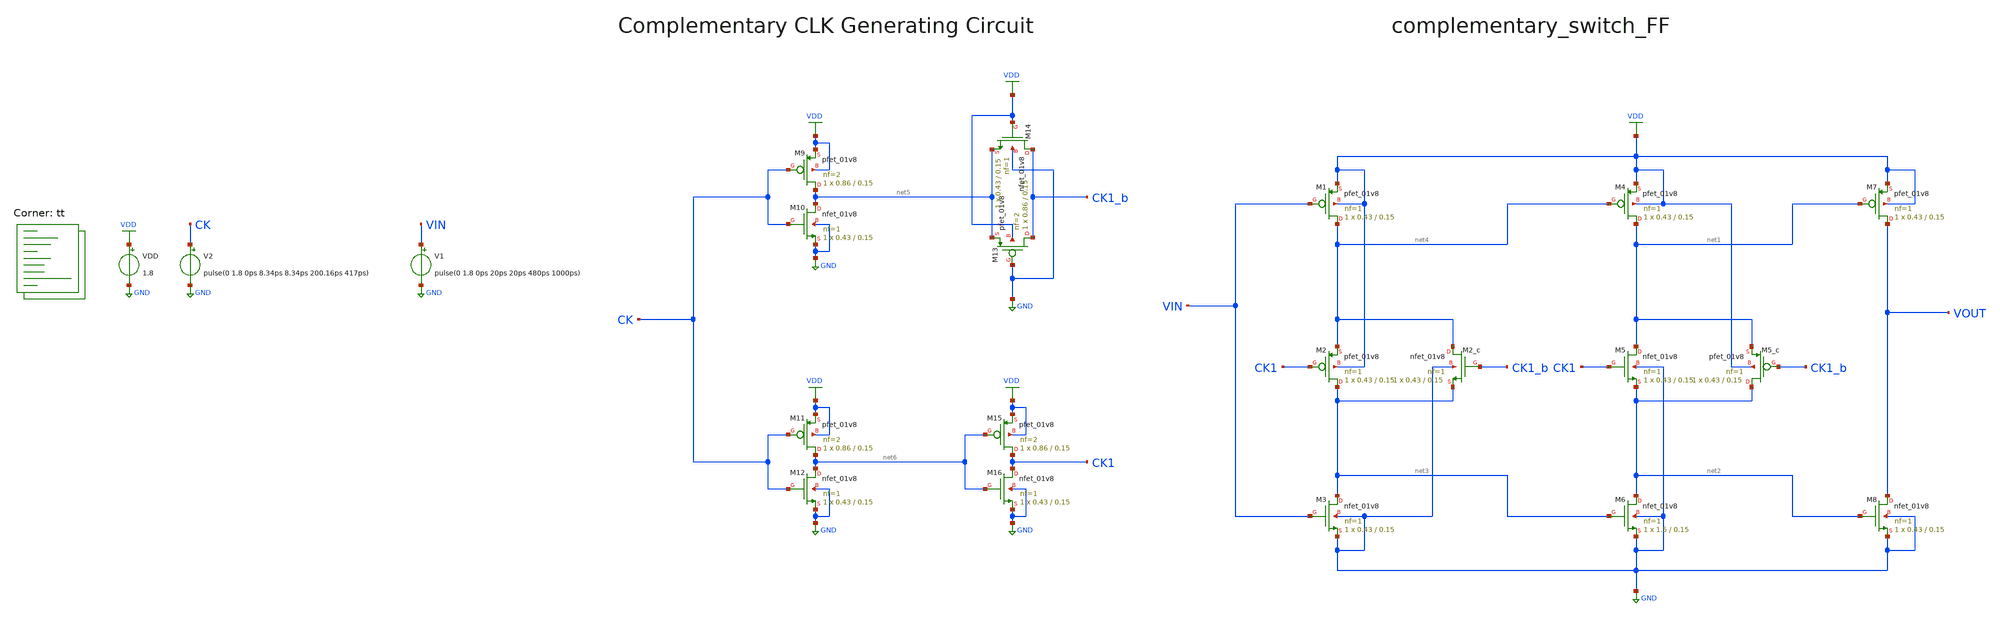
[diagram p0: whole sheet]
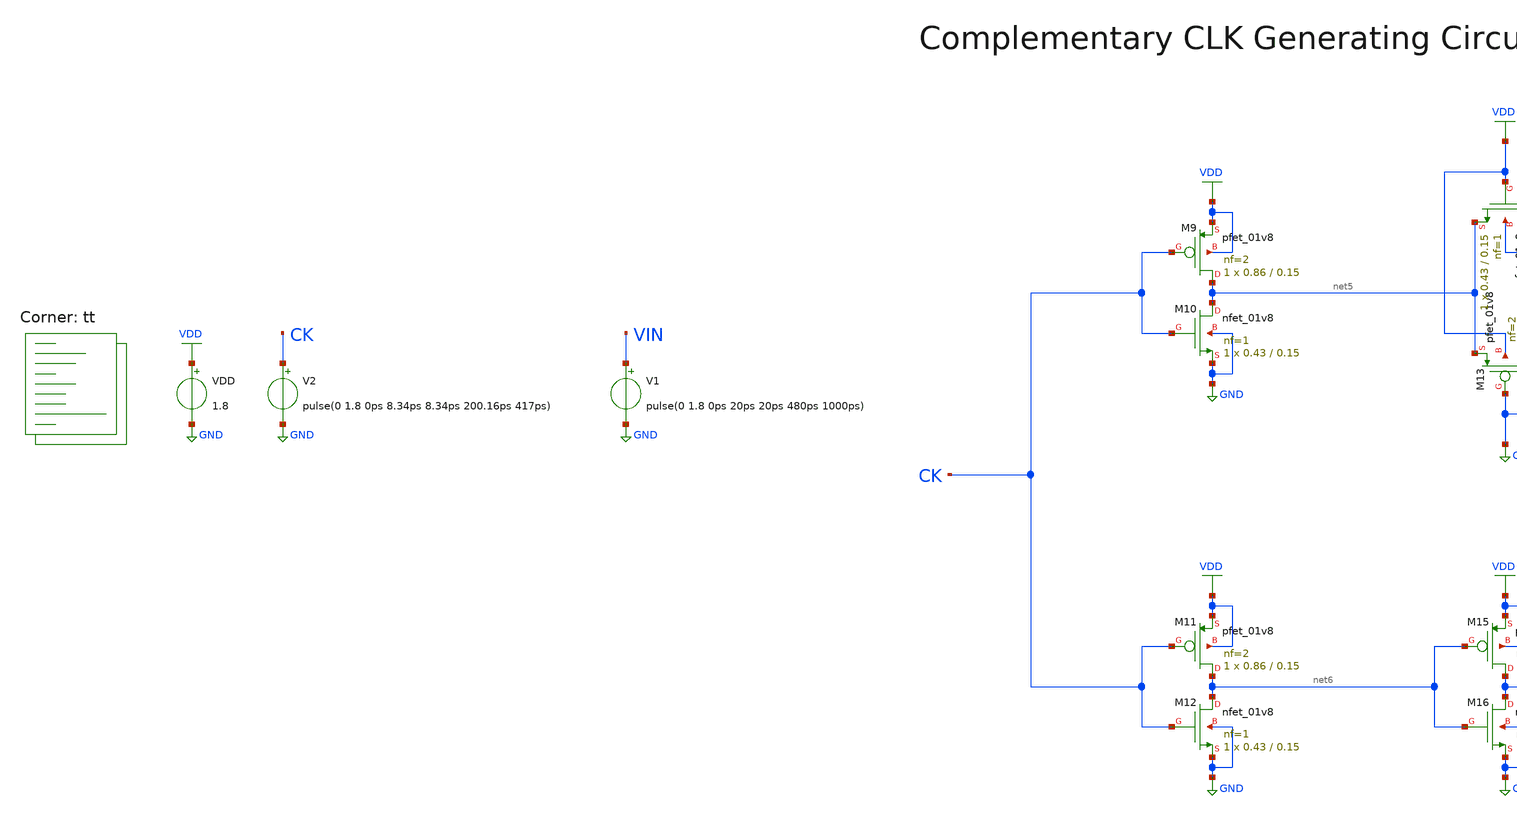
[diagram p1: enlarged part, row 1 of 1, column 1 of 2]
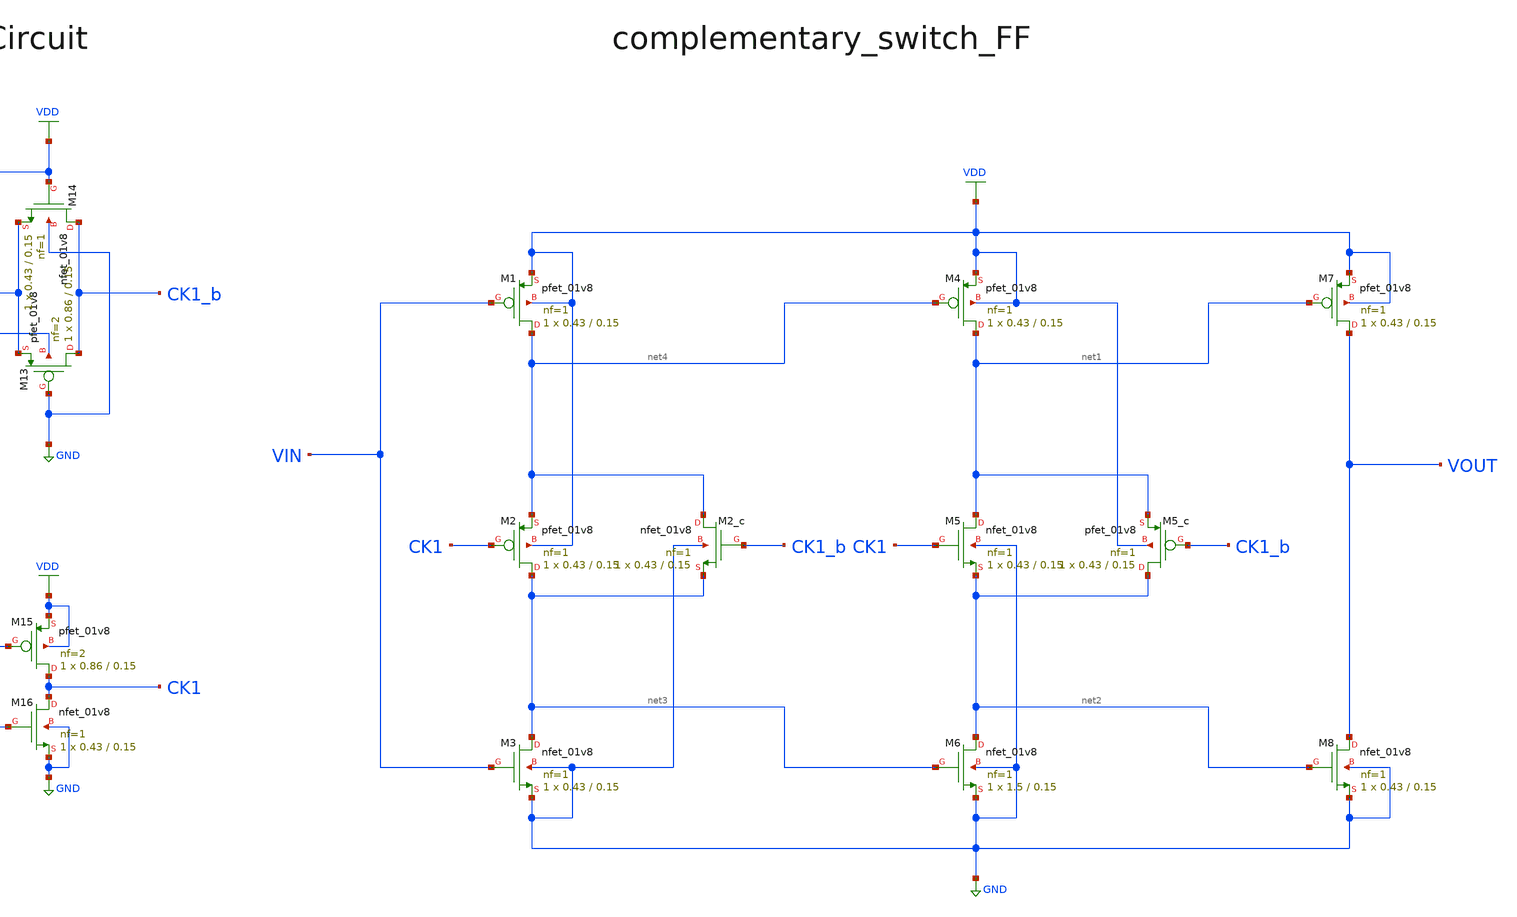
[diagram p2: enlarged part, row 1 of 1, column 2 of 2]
** sch_path: projects/pll/divider/xschem_ngspice/tb_FF_comp_sw.sch
**.subckt tb_FF_comp_sw
VDD VDD GND 1.8
V2 CK GND pulse(0 1.8 0ps 8.34ps 8.34ps 200.16ps 417ps)
XM7 VOUT net1 VDD VDD sky130_fd_pr__pfet_01v8 L=0.15 W=0.43 nf=1 ad='int((nf+1)/2) * W/nf * 0.29' as='int((nf+2)/2) * W/nf * 0.29'
+ pd='2*int((nf+1)/2) * (W/nf + 0.29)' ps='2*int((nf+2)/2) * (W/nf + 0.29)' nrd='0.29 / W' nrs='0.29 / W'
+ sa=0 sb=0 sd=0 mult=1 m=1
XM5 net1 CK1 net2 GND sky130_fd_pr__nfet_01v8 L=0.15 W=0.43 nf=1 ad='int((nf+1)/2) * W/nf * 0.29' as='int((nf+2)/2) * W/nf * 0.29'
+ pd='2*int((nf+1)/2) * (W/nf + 0.29)' ps='2*int((nf+2)/2) * (W/nf + 0.29)' nrd='0.29 / W' nrs='0.29 / W'
+ sa=0 sb=0 sd=0 mult=1 m=1
XM8 VOUT net2 GND GND sky130_fd_pr__nfet_01v8 L=0.15 W=0.43 nf=1 ad='int((nf+1)/2) * W/nf * 0.29' as='int((nf+2)/2) * W/nf * 0.29'
+ pd='2*int((nf+1)/2) * (W/nf + 0.29)' ps='2*int((nf+2)/2) * (W/nf + 0.29)' nrd='0.29 / W' nrs='0.29 / W'
+ sa=0 sb=0 sd=0 mult=1 m=1
XM4 net1 net4 VDD VDD sky130_fd_pr__pfet_01v8 L=0.15 W=0.43 nf=1 ad='int((nf+1)/2) * W/nf * 0.29' as='int((nf+2)/2) * W/nf * 0.29'
+ pd='2*int((nf+1)/2) * (W/nf + 0.29)' ps='2*int((nf+2)/2) * (W/nf + 0.29)' nrd='0.29 / W' nrs='0.29 / W'
+ sa=0 sb=0 sd=0 mult=1 m=1
XM6 net2 net3 GND GND sky130_fd_pr__nfet_01v8 L=0.15 W=1.5 nf=1 ad='int((nf+1)/2) * W/nf * 0.29' as='int((nf+2)/2) * W/nf * 0.29'
+ pd='2*int((nf+1)/2) * (W/nf + 0.29)' ps='2*int((nf+2)/2) * (W/nf + 0.29)' nrd='0.29 / W' nrs='0.29 / W'
+ sa=0 sb=0 sd=0 mult=1 m=1
XM1 net4 VIN VDD VDD sky130_fd_pr__pfet_01v8 L=0.15 W=0.43 nf=1 ad='int((nf+1)/2) * W/nf * 0.29' as='int((nf+2)/2) * W/nf * 0.29'
+ pd='2*int((nf+1)/2) * (W/nf + 0.29)' ps='2*int((nf+2)/2) * (W/nf + 0.29)' nrd='0.29 / W' nrs='0.29 / W'
+ sa=0 sb=0 sd=0 mult=1 m=1
XM3 net3 VIN GND GND sky130_fd_pr__nfet_01v8 L=0.15 W=0.43 nf=1 ad='int((nf+1)/2) * W/nf * 0.29' as='int((nf+2)/2) * W/nf * 0.29'
+ pd='2*int((nf+1)/2) * (W/nf + 0.29)' ps='2*int((nf+2)/2) * (W/nf + 0.29)' nrd='0.29 / W' nrs='0.29 / W'
+ sa=0 sb=0 sd=0 mult=1 m=1
XM2 net3 CK1 net4 VDD sky130_fd_pr__pfet_01v8 L=0.15 W=0.43 nf=1 ad='int((nf+1)/2) * W/nf * 0.29' as='int((nf+2)/2) * W/nf * 0.29'
+ pd='2*int((nf+1)/2) * (W/nf + 0.29)' ps='2*int((nf+2)/2) * (W/nf + 0.29)' nrd='0.29 / W' nrs='0.29 / W'
+ sa=0 sb=0 sd=0 mult=1 m=1
XM5_c net2 CK1_b net1 VDD sky130_fd_pr__pfet_01v8 L=0.15 W=0.43 nf=1 ad='int((nf+1)/2) * W/nf * 0.29'
+ as='int((nf+2)/2) * W/nf * 0.29' pd='2*int((nf+1)/2) * (W/nf + 0.29)' ps='2*int((nf+2)/2) * (W/nf + 0.29)'
+ nrd='0.29 / W' nrs='0.29 / W' sa=0 sb=0 sd=0 mult=1 m=1
XM2_c net4 CK1_b net3 GND sky130_fd_pr__nfet_01v8 L=0.15 W=0.43 nf=1 ad='int((nf+1)/2) * W/nf * 0.29'
+ as='int((nf+2)/2) * W/nf * 0.29' pd='2*int((nf+1)/2) * (W/nf + 0.29)' ps='2*int((nf+2)/2) * (W/nf + 0.29)'
+ nrd='0.29 / W' nrs='0.29 / W' sa=0 sb=0 sd=0 mult=1 m=1
XM13 CK1_b GND net5 VDD sky130_fd_pr__pfet_01v8 L=0.15 W=0.86 nf=2 ad='int((nf+1)/2) * W/nf * 0.29' as='int((nf+2)/2) * W/nf * 0.29'
+ pd='2*int((nf+1)/2) * (W/nf + 0.29)' ps='2*int((nf+2)/2) * (W/nf + 0.29)' nrd='0.29 / W' nrs='0.29 / W'
+ sa=0 sb=0 sd=0 mult=1 m=1
XM14 CK1_b VDD net5 GND sky130_fd_pr__nfet_01v8 L=0.15 W=0.43 nf=1 ad='int((nf+1)/2) * W/nf * 0.29' as='int((nf+2)/2) * W/nf * 0.29'
+ pd='2*int((nf+1)/2) * (W/nf + 0.29)' ps='2*int((nf+2)/2) * (W/nf + 0.29)' nrd='0.29 / W' nrs='0.29 / W'
+ sa=0 sb=0 sd=0 mult=1 m=1
XM15 CK1 net6 VDD VDD sky130_fd_pr__pfet_01v8 L=0.15 W=0.86 nf=2 ad='int((nf+1)/2) * W/nf * 0.29' as='int((nf+2)/2) * W/nf * 0.29'
+ pd='2*int((nf+1)/2) * (W/nf + 0.29)' ps='2*int((nf+2)/2) * (W/nf + 0.29)' nrd='0.29 / W' nrs='0.29 / W'
+ sa=0 sb=0 sd=0 mult=1 m=1
XM16 CK1 net6 GND GND sky130_fd_pr__nfet_01v8 L=0.15 W=0.43 nf=1 ad='int((nf+1)/2) * W/nf * 0.29' as='int((nf+2)/2) * W/nf * 0.29'
+ pd='2*int((nf+1)/2) * (W/nf + 0.29)' ps='2*int((nf+2)/2) * (W/nf + 0.29)' nrd='0.29 / W' nrs='0.29 / W'
+ sa=0 sb=0 sd=0 mult=1 m=1
XM11 net6 CK VDD VDD sky130_fd_pr__pfet_01v8 L=0.15 W=0.86 nf=2 ad='int((nf+1)/2) * W/nf * 0.29' as='int((nf+2)/2) * W/nf * 0.29'
+ pd='2*int((nf+1)/2) * (W/nf + 0.29)' ps='2*int((nf+2)/2) * (W/nf + 0.29)' nrd='0.29 / W' nrs='0.29 / W'
+ sa=0 sb=0 sd=0 mult=1 m=1
XM12 net6 CK GND GND sky130_fd_pr__nfet_01v8 L=0.15 W=0.43 nf=1 ad='int((nf+1)/2) * W/nf * 0.29' as='int((nf+2)/2) * W/nf * 0.29'
+ pd='2*int((nf+1)/2) * (W/nf + 0.29)' ps='2*int((nf+2)/2) * (W/nf + 0.29)' nrd='0.29 / W' nrs='0.29 / W'
+ sa=0 sb=0 sd=0 mult=1 m=1
XM9 net5 CK VDD VDD sky130_fd_pr__pfet_01v8 L=0.15 W=0.86 nf=2 ad='int((nf+1)/2) * W/nf * 0.29' as='int((nf+2)/2) * W/nf * 0.29'
+ pd='2*int((nf+1)/2) * (W/nf + 0.29)' ps='2*int((nf+2)/2) * (W/nf + 0.29)' nrd='0.29 / W' nrs='0.29 / W'
+ sa=0 sb=0 sd=0 mult=1 m=1
XM10 net5 CK GND GND sky130_fd_pr__nfet_01v8 L=0.15 W=0.43 nf=1 ad='int((nf+1)/2) * W/nf * 0.29' as='int((nf+2)/2) * W/nf * 0.29'
+ pd='2*int((nf+1)/2) * (W/nf + 0.29)' ps='2*int((nf+2)/2) * (W/nf + 0.29)' nrd='0.29 / W' nrs='0.29 / W'
+ sa=0 sb=0 sd=0 mult=1 m=1
V1 VIN GND pulse(0 1.8 0ps 20ps 20ps 480ps 1000ps)
**** begin user architecture code



.option method=gear
.option wnflag=1

.control

  save all
  tran 5p 20n
  remzerovec
  write tb_FF_comp_sw.raw
  * set appendwrite

.endc



.lib $::SKYWATER_MODELS/sky130.lib.spice tt
**** end user architecture code
**.ends
.GLOBAL GND
.GLOBAL VDD
.end
